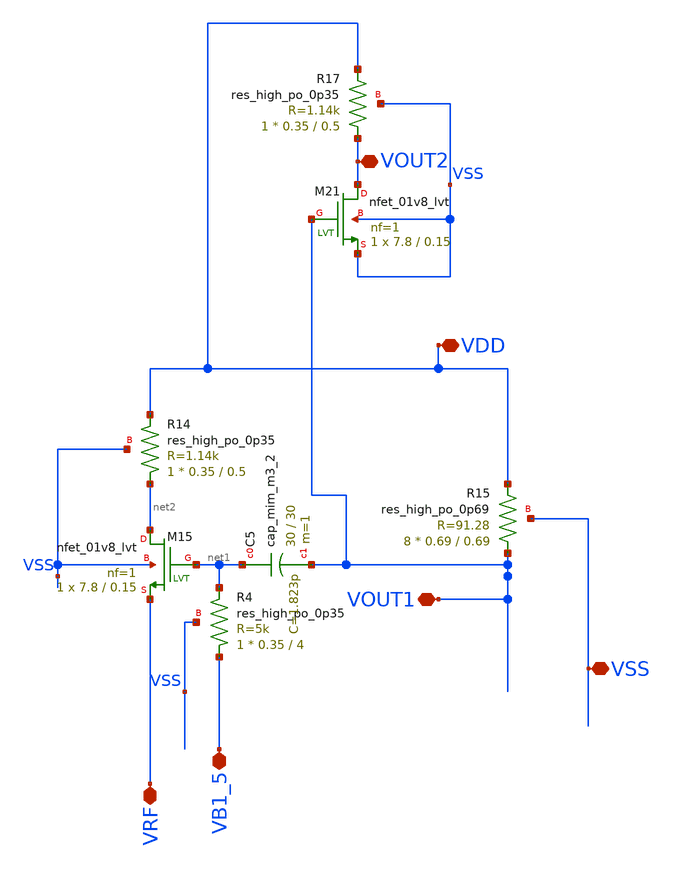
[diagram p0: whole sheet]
** sch_path: xschem/xschem4_sic_oct_20/partition2.sch
**.subckt partition2 VDD VOUT1 VOUT2 VB1_5 VSS VRF
*.iopin VDD
*.iopin VOUT1
*.iopin VOUT2
*.iopin VB1_5
*.iopin VSS
*.iopin VRF
XR4 VB1_5 net1 VSS sky130_fd_pr__res_high_po_0p35 L=4 mult=1 m=1
XC5 net1 VOUT1 sky130_fd_pr__cap_mim_m3_2 W=30 L=30 MF=1 m=1
XM15 net2 net1 VRF VSS sky130_fd_pr__nfet_01v8_lvt L=0.15 W=7.8 nf=1 ad='int((nf+1)/2) * W/nf * 0.29'
+ as='int((nf+2)/2) * W/nf * 0.29' pd='2*int((nf+1)/2) * (W/nf + 0.29)' ps='2*int((nf+2)/2) * (W/nf + 0.29)'
+ nrd='0.29 / W' nrs='0.29 / W' sa=0 sb=0 sd=0 mult=1 m=1
XR14 net2 VDD VSS sky130_fd_pr__res_high_po_0p35 L=0.5 mult=1 m=1
XR15 VOUT1 VDD VSS sky130_fd_pr__res_high_po_0p69 L=0.69 mult=8 m=8
XM21 VOUT2 VOUT1 VSS VSS sky130_fd_pr__nfet_01v8_lvt L=0.15 W=7.8 nf=1 ad='int((nf+1)/2) * W/nf * 0.29'
+ as='int((nf+2)/2) * W/nf * 0.29' pd='2*int((nf+1)/2) * (W/nf + 0.29)' ps='2*int((nf+2)/2) * (W/nf + 0.29)'
+ nrd='0.29 / W' nrs='0.29 / W' sa=0 sb=0 sd=0 mult=1 m=1
XR17 VOUT2 VDD VSS sky130_fd_pr__res_high_po_0p35 L=0.5 mult=1 m=1
**.ends
.end
